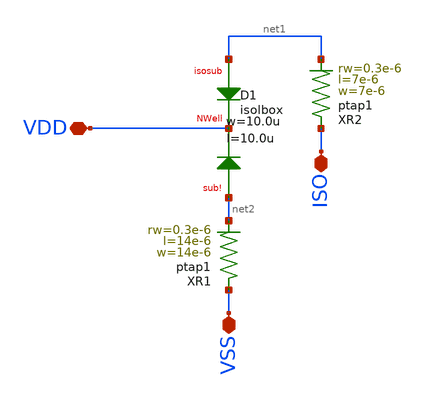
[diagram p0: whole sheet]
** sch_path: deepNWell/schematic/sg13_nwell_sch.sch
**.subckt sg13_nwell_sch VSS ISO VDD
*.iopin VSS
*.iopin ISO
*.iopin VDD
XD1 net1 VDD net2 isolbox l=10.0u w=10.0u
XR1 VSS net2 ptap1 R=4.159 w=14e-6 l=14e-6 rw=0.3e-6
XR2 ISO net1 ptap1 R=8.504 w=7e-6 l=7e-6 rw=0.3e-6
**.ends
.end
